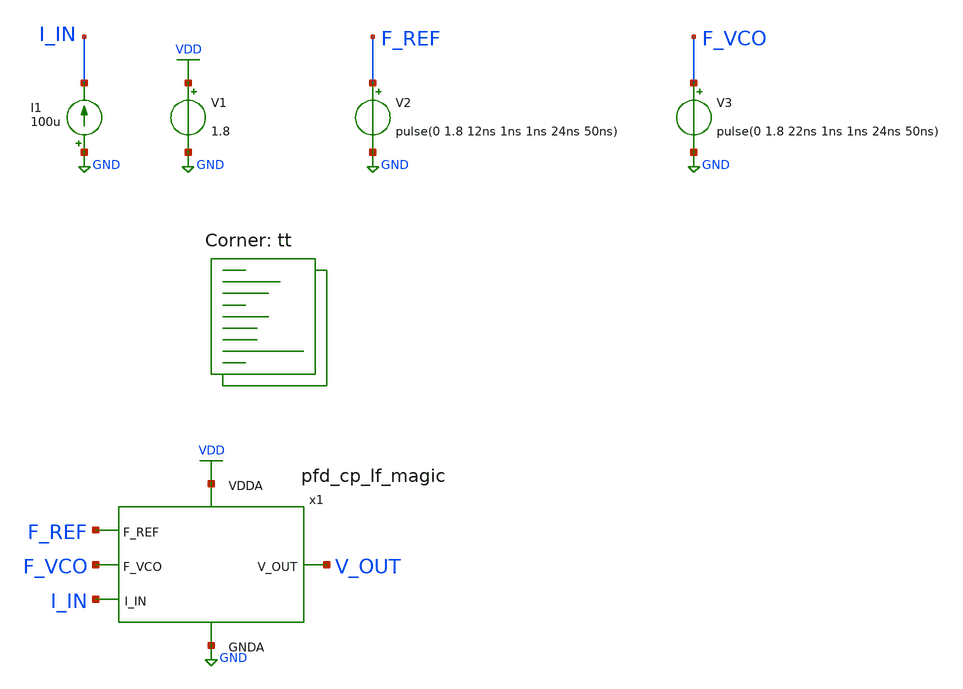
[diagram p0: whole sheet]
** sch_path: projects/pll/charge_pump/magic/pfd_charge_pump_magic_4.sch
**.subckt pfd_charge_pump_magic_4
V1 VDD GND 1.8
V2 F_REF GND pulse(0 1.8 12ns 1ns 1ns 24ns 50ns)
V3 F_VCO GND pulse(0 1.8 22ns 1ns 1ns 24ns 50ns)
I1 GND I_IN 100u
x1 V_OUT VDD GND F_REF F_VCO I_IN pfd_cp_lf_magic
**** begin user architecture code
.lib $::SKYWATER_MODELS/sky130.lib.spice tt



.include /foss/designs/my_design/projects/pll/charge_pump/magic/pfd_cp_lf_magic.spice
.include /foss/designs/my_design/projects/pll/charge_pump/magic/pfd_cp_magic.spice
.include /foss/designs/my_design/projects/pll/charge_pump/magic/pfd_cp_input_magic.spice
.include /foss/designs/my_design/projects/pll/charge_pump/magic/charge_pump_magic.spice
.include /foss/designs/my_design/projects/pll/charge_pump/magic/rail_to_rail_opamp_magic.spice
.include /foss/designs/my_design/projects/pll/charge_pump/magic/loop_filter_magic.spice

.option method=gear
.option wnflag=1
.option savecurrents

* V_out initial voltage value for the F_VCO delay of 2ns  (leading)
* .ic v(v_out) = 1.8

* V_out initial voltage value for the F_VCO delay of 12ns (lock condition)
* .ic v(v_out) = 0.9

* V_out initial voltage value for the F_VCO delay of 22ns (lagging)
.ic v(v_out) = 0.0

.control
  save v(f_ref) save v(f_vco) save v(i_in) save v(up_pfd) v(down_pfd) v(up_pfd_b) v(down_pfd_b)
+ v(up) v(up_b) v(down) v(down_b) v(x) v(opamp_out) v(up_input) v(down_input) v(down_gate) v(v_out)
  * save all

  * timestep for exact simulation results
  * tran 5ps 0.5us

  * timestep for faster simulation results
  tran 50ps 0.5us

  remzerovec
  write pfd_charge_pump_magic_4_2.raw
  set appendwrite

.endc



**** end user architecture code
**.ends
.GLOBAL GND
.GLOBAL VDD
.end
